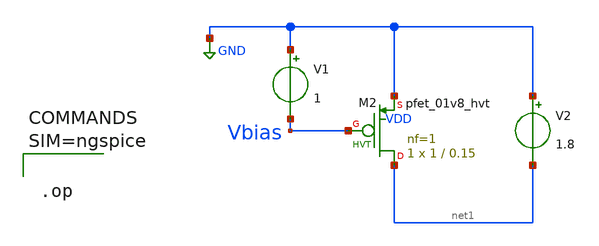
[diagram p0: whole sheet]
** sch_path: xschem/Polarizzazione.sch
**.subckt Polarizzazione
XM2 net1 Vbias GND VDD sky130_fd_pr__pfet_01v8_hvt L=0.15 W=1 nf=1 ad='int((nf+1)/2) * W/nf * 0.29' as='int((nf+2)/2) * W/nf * 0.29'
+ pd='2*int((nf+1)/2) * (W/nf + 0.29)' ps='2*int((nf+2)/2) * (W/nf + 0.29)' nrd='0.29 / W' nrs='0.29 / W'
+ sa=0 sb=0 sd=0 mult=1 m=1
V1 GND Vbias 1
V2 GND net1 1.8
**** begin user architecture code

** opencircuitdesign pdks install
.lib $::SKYWATER_MODELS/sky130.lib.spice tt





.op



**** end user architecture code
**.ends
.GLOBAL GND
.end
